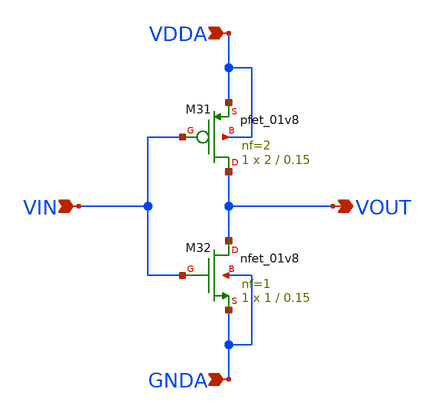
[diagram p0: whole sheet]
** sch_path: projects/pll/divider/xschem_ngspice/inverter.sch
**.subckt inverter VIN VDDA GNDA VOUT
*.ipin VIN
*.ipin VDDA
*.ipin GNDA
*.opin VOUT
XM31 VOUT VIN VDDA VDDA sky130_fd_pr__pfet_01v8 L=0.15 W=2 nf=2 ad='int((nf+1)/2) * W/nf * 0.29' as='int((nf+2)/2) * W/nf * 0.29'
+ pd='2*int((nf+1)/2) * (W/nf + 0.29)' ps='2*int((nf+2)/2) * (W/nf + 0.29)' nrd='0.29 / W' nrs='0.29 / W'
+ sa=0 sb=0 sd=0 mult=1 m=1
XM32 VOUT VIN GNDA GNDA sky130_fd_pr__nfet_01v8 L=0.15 W=1 nf=1 ad='int((nf+1)/2) * W/nf * 0.29' as='int((nf+2)/2) * W/nf * 0.29'
+ pd='2*int((nf+1)/2) * (W/nf + 0.29)' ps='2*int((nf+2)/2) * (W/nf + 0.29)' nrd='0.29 / W' nrs='0.29 / W'
+ sa=0 sb=0 sd=0 mult=1 m=1
**.ends
.end
